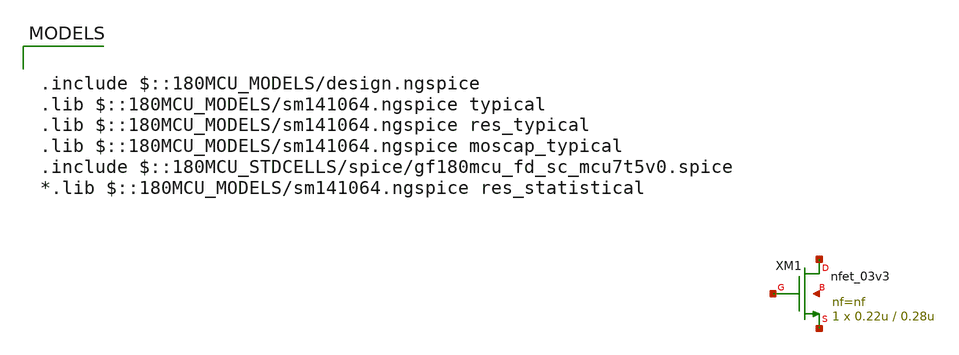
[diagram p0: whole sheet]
** sch_path: xschem/untitled-1.sch
**.subckt untitled-1
XM1 net1 net2 net3 net4 nfet_03v3 L=0.28u W=0.22u nf=nf ad='int((nf+1)/2) * W/nf * 0.18u' as='int((nf+2)/2) * W/nf * 0.18u'
+ pd='2*int((nf+1)/2) * (W/nf + 0.18u)' ps='2*int((nf+2)/2) * (W/nf + 0.18u)' nrd='0.18u / W' nrs='0.18u / W'
+ sa=0 sb=0 sd=0 m=1
**** begin user architecture code


.param nf=1
.options savecurrents
.control

.endc

.save all



.include $::180MCU_MODELS/design.ngspice
.lib $::180MCU_MODELS/sm141064.ngspice typical
.lib $::180MCU_MODELS/sm141064.ngspice res_typical
.lib $::180MCU_MODELS/sm141064.ngspice moscap_typical
.include $::180MCU_STDCELLS/spice/gf180mcu_fd_sc_mcu7t5v0.spice
*.lib $::180MCU_MODELS/sm141064.ngspice res_statistical

**** end user architecture code
**.ends
.end
